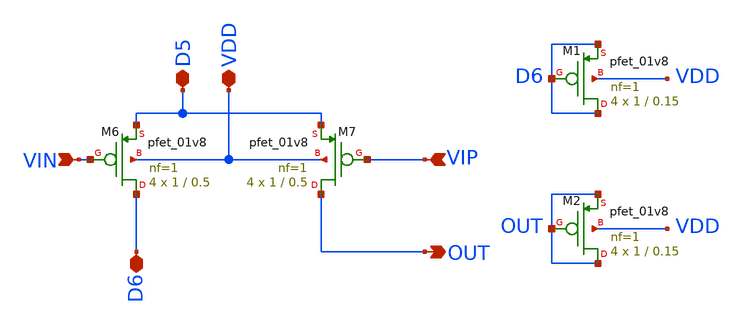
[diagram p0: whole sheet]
** sch_path: opamp/mag/pmoscs67.sch
**.subckt pmoscs67 VIP VIN OUT VDD D6 D5
*.ipin VIP
*.ipin VIN
*.opin OUT
*.iopin VDD
*.iopin D6
*.iopin D5
XM1 D6 D6 D6 VDD sky130_fd_pr__pfet_01v8 L=0.15 W=1 nf=1 ad='int((nf+1)/2) * W/nf * 0.29' as='int((nf+2)/2) * W/nf * 0.29'
+ pd='2*int((nf+1)/2) * (W/nf + 0.29)' ps='2*int((nf+2)/2) * (W/nf + 0.29)' nrd='0.29 / W' nrs='0.29 / W'
+ sa=0 sb=0 sd=0 mult=4 m=4
XM6 D6 VIN D5 VDD sky130_fd_pr__pfet_01v8 L=0.5 W=1 nf=1 ad='int((nf+1)/2) * W/nf * 0.29' as='int((nf+2)/2) * W/nf * 0.29'
+ pd='2*int((nf+1)/2) * (W/nf + 0.29)' ps='2*int((nf+2)/2) * (W/nf + 0.29)' nrd='0.29 / W' nrs='0.29 / W'
+ sa=0 sb=0 sd=0 mult=4 m=4
XM7 OUT VIP D5 VDD sky130_fd_pr__pfet_01v8 L=0.5 W=1 nf=1 ad='int((nf+1)/2) * W/nf * 0.29' as='int((nf+2)/2) * W/nf * 0.29'
+ pd='2*int((nf+1)/2) * (W/nf + 0.29)' ps='2*int((nf+2)/2) * (W/nf + 0.29)' nrd='0.29 / W' nrs='0.29 / W'
+ sa=0 sb=0 sd=0 mult=4 m=4
XM2 OUT OUT OUT VDD sky130_fd_pr__pfet_01v8 L=0.15 W=1 nf=1 ad='int((nf+1)/2) * W/nf * 0.29' as='int((nf+2)/2) * W/nf * 0.29'
+ pd='2*int((nf+1)/2) * (W/nf + 0.29)' ps='2*int((nf+2)/2) * (W/nf + 0.29)' nrd='0.29 / W' nrs='0.29 / W'
+ sa=0 sb=0 sd=0 mult=4 m=4
**.ends
.end
